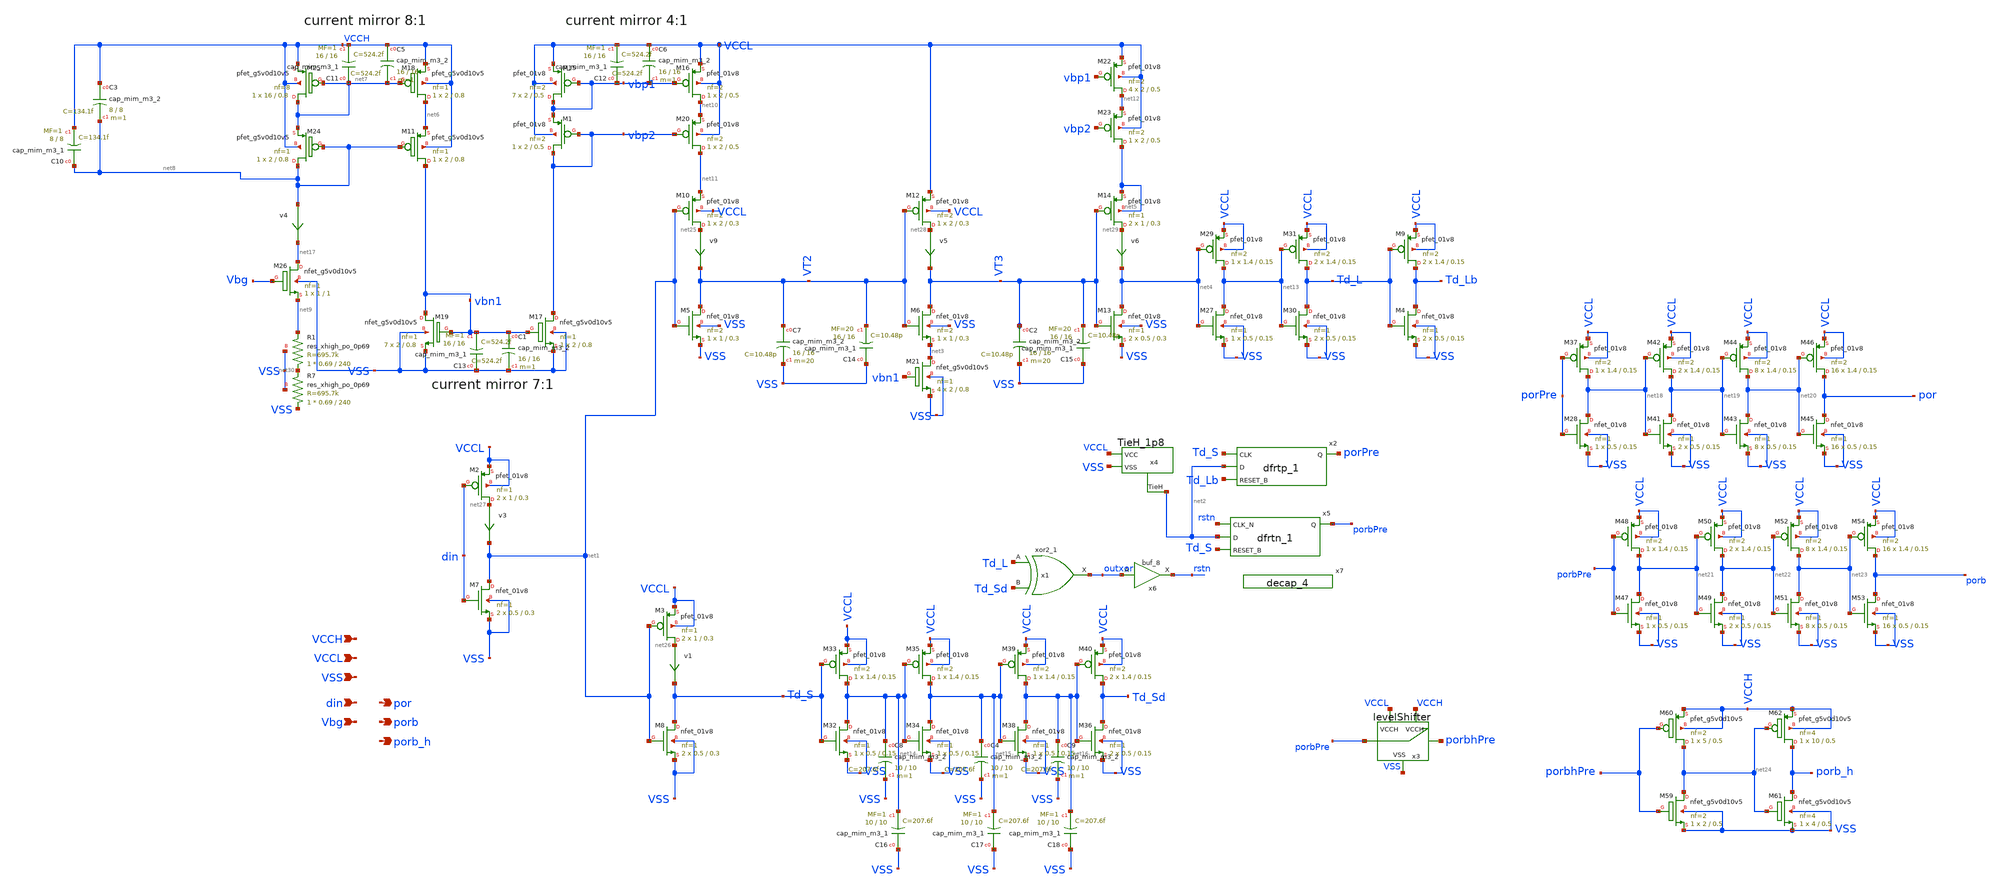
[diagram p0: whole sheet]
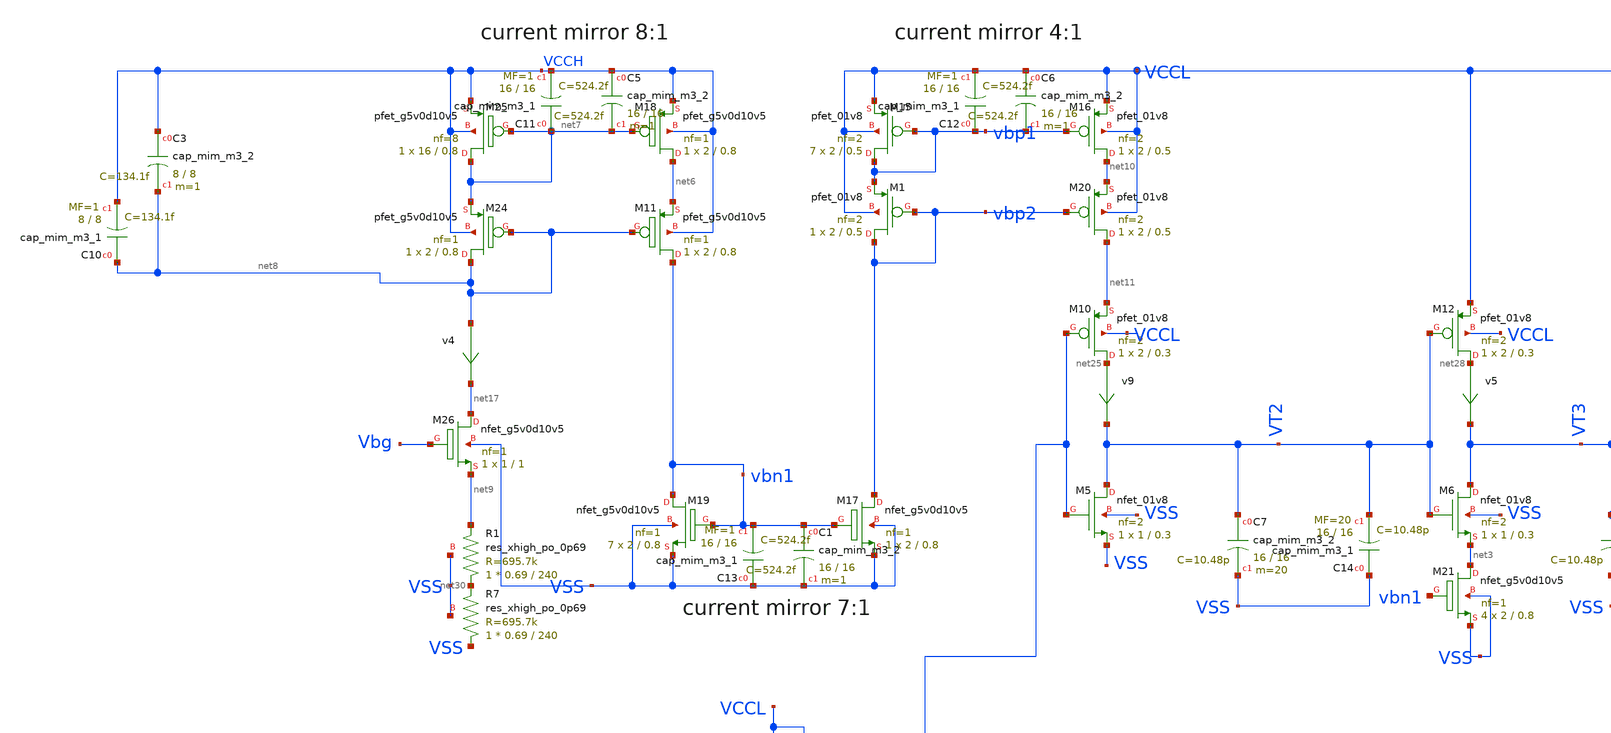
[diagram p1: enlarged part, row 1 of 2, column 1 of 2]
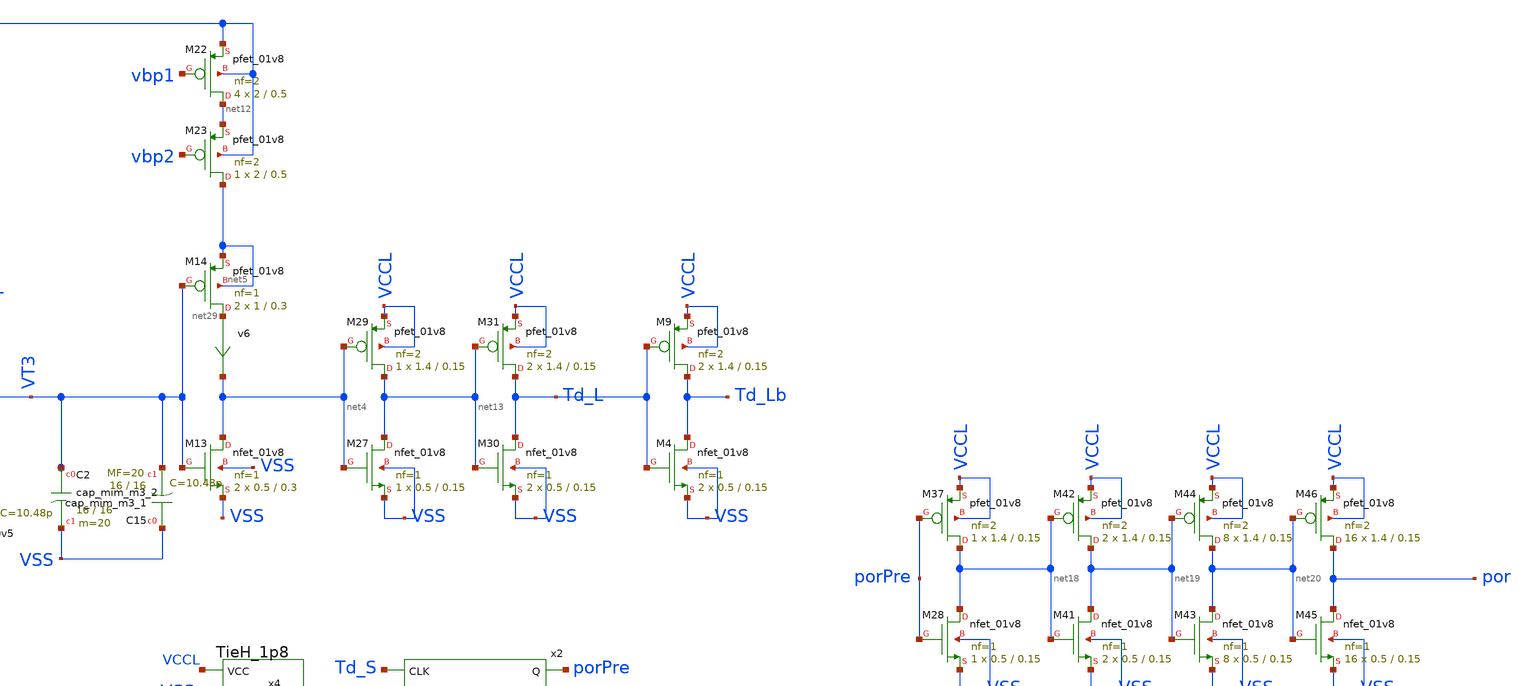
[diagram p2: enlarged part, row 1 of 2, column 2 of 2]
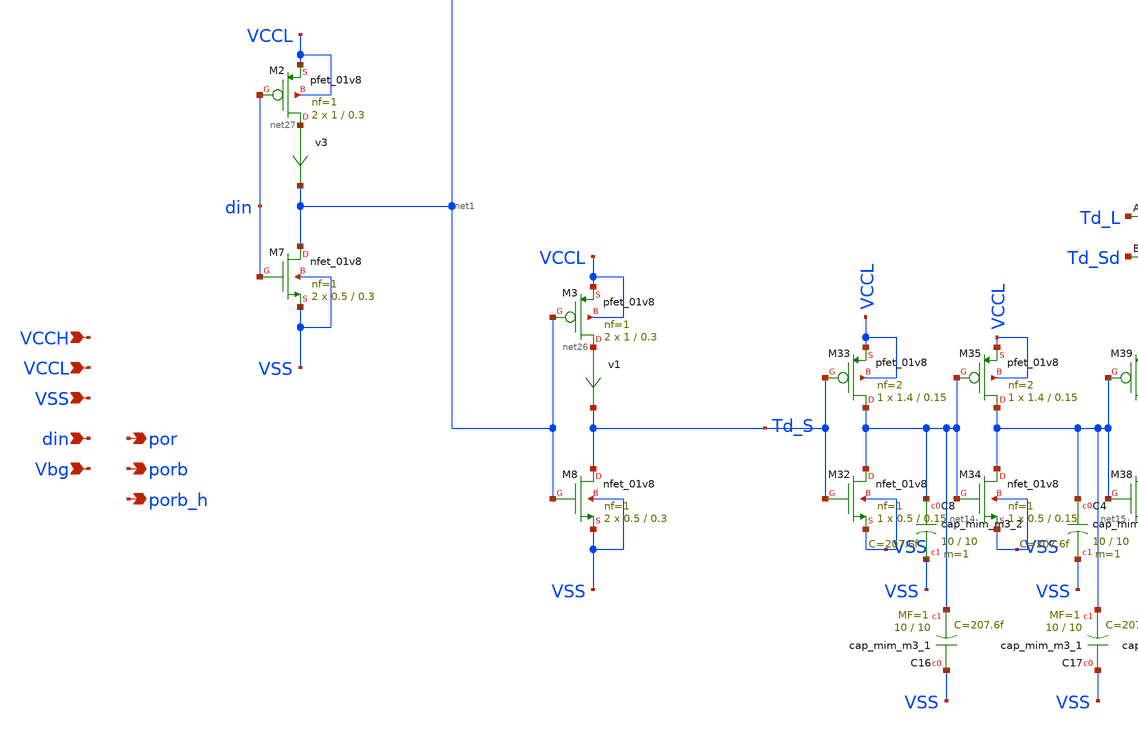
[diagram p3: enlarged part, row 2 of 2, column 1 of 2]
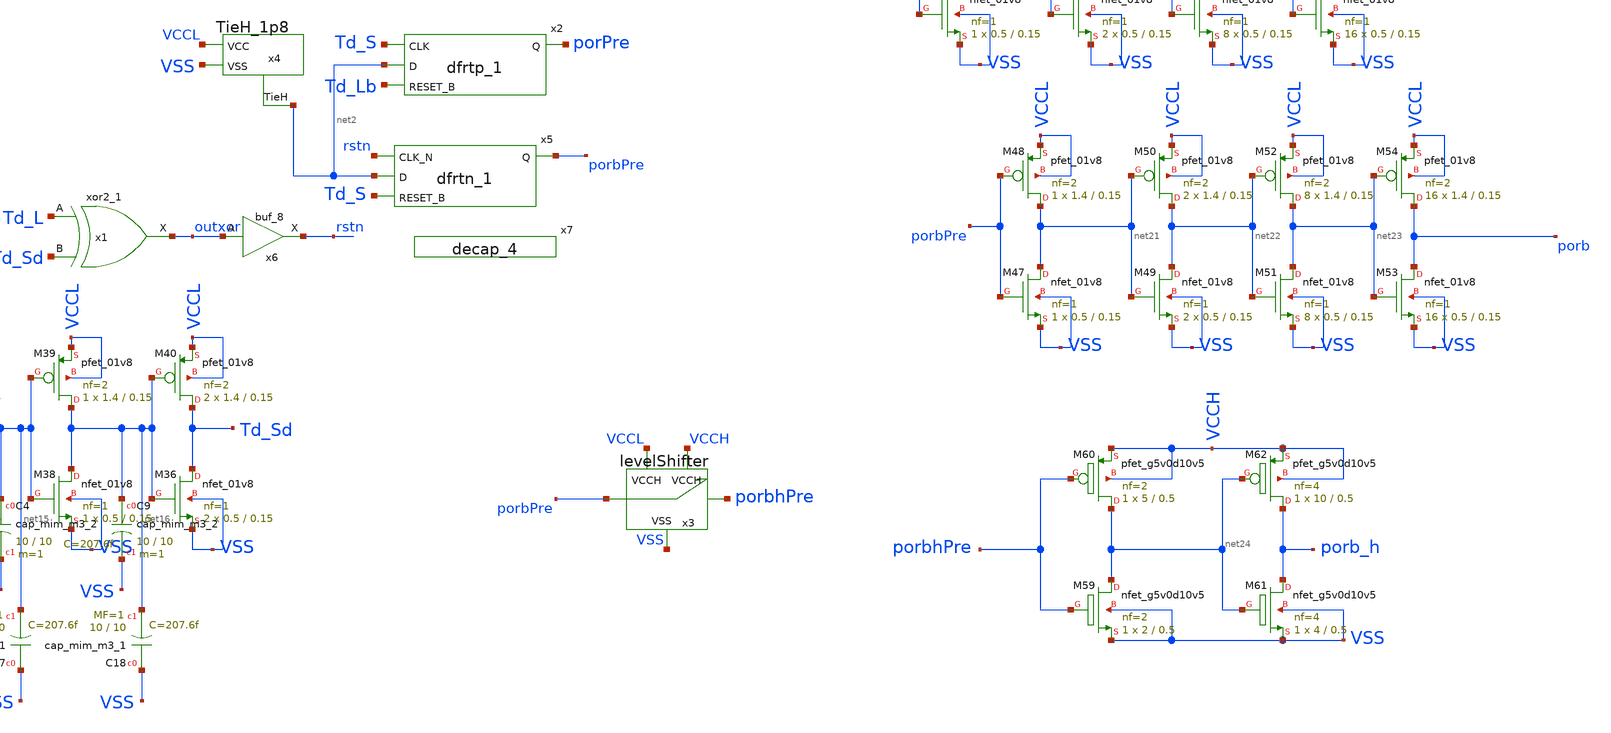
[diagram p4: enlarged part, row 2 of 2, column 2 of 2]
** sch_path: xschem_sim/delayPulse_final.sch
**.subckt delayPulse_final VCCL VSS din Vbg por VCCH porb porb_h
*.ipin VCCL
*.ipin VSS
*.ipin din
*.ipin Vbg
*.opin por
*.ipin VCCH
*.opin porb
*.opin porb_h
v9 net25 VT2 0
.save i(v9)
v1 net26 Td_S 0
.save i(v1)
v3 net27 net1 0
.save i(v3)
x1 Td_L Td_Sd VSS VSS VCCL VCCL outxor sky130_fd_sc_ls__xor2_1
x3 porbPre porbhPre VCCL VSS VCCH levelShifter
XM2 net27 din VCCL VCCL sky130_fd_pr__pfet_01v8 L=0.3 W=1 nf=1 ad='int((nf+1)/2) * W/nf * 0.29' as='int((nf+2)/2) * W/nf * 0.29'
+ pd='2*int((nf+1)/2) * (W/nf + 0.29)' ps='2*int((nf+2)/2) * (W/nf + 0.29)' nrd='0.29 / W' nrs='0.29 / W'
+ sa=0 sb=0 sd=0 mult=2 m=2
XM3 net26 net1 VCCL VCCL sky130_fd_pr__pfet_01v8 L=0.3 W=1 nf=1 ad='int((nf+1)/2) * W/nf * 0.29' as='int((nf+2)/2) * W/nf * 0.29'
+ pd='2*int((nf+1)/2) * (W/nf + 0.29)' ps='2*int((nf+2)/2) * (W/nf + 0.29)' nrd='0.29 / W' nrs='0.29 / W'
+ sa=0 sb=0 sd=0 mult=2 m=2
XM5 VT2 net1 VSS VSS sky130_fd_pr__nfet_01v8 L=0.3 W=1 nf=2 ad='int((nf+1)/2) * W/nf * 0.29' as='int((nf+2)/2) * W/nf * 0.29'
+ pd='2*int((nf+1)/2) * (W/nf + 0.29)' ps='2*int((nf+2)/2) * (W/nf + 0.29)' nrd='0.29 / W' nrs='0.29 / W'
+ sa=0 sb=0 sd=0 mult=1 m=1
XM7 net1 din VSS VSS sky130_fd_pr__nfet_01v8 L=0.3 W=0.5 nf=1 ad='int((nf+1)/2) * W/nf * 0.29' as='int((nf+2)/2) * W/nf * 0.29'
+ pd='2*int((nf+1)/2) * (W/nf + 0.29)' ps='2*int((nf+2)/2) * (W/nf + 0.29)' nrd='0.29 / W' nrs='0.29 / W'
+ sa=0 sb=0 sd=0 mult=2 m=2
XM8 Td_S net1 VSS VSS sky130_fd_pr__nfet_01v8 L=0.3 W=0.5 nf=1 ad='int((nf+1)/2) * W/nf * 0.29' as='int((nf+2)/2) * W/nf * 0.29'
+ pd='2*int((nf+1)/2) * (W/nf + 0.29)' ps='2*int((nf+2)/2) * (W/nf + 0.29)' nrd='0.29 / W' nrs='0.29 / W'
+ sa=0 sb=0 sd=0 mult=2 m=2
XM10 net25 net1 net11 VCCL sky130_fd_pr__pfet_01v8 L=0.3 W=2 nf=2 ad='int((nf+1)/2) * W/nf * 0.29' as='int((nf+2)/2) * W/nf * 0.29'
+ pd='2*int((nf+1)/2) * (W/nf + 0.29)' ps='2*int((nf+2)/2) * (W/nf + 0.29)' nrd='0.29 / W' nrs='0.29 / W'
+ sa=0 sb=0 sd=0 mult=1 m=1
v5 net28 VT3 0
.save i(v5)
v6 net29 net4 0
.save i(v6)
XM13 net4 VT3 VSS VSS sky130_fd_pr__nfet_01v8 L=0.3 W=0.5 nf=1 ad='int((nf+1)/2) * W/nf * 0.29' as='int((nf+2)/2) * W/nf * 0.29'
+ pd='2*int((nf+1)/2) * (W/nf + 0.29)' ps='2*int((nf+2)/2) * (W/nf + 0.29)' nrd='0.29 / W' nrs='0.29 / W'
+ sa=0 sb=0 sd=0 mult=2 m=2
XM14 net29 VT3 net5 net5 sky130_fd_pr__pfet_01v8 L=0.3 W=1 nf=1 ad='int((nf+1)/2) * W/nf * 0.29' as='int((nf+2)/2) * W/nf * 0.29'
+ pd='2*int((nf+1)/2) * (W/nf + 0.29)' ps='2*int((nf+2)/2) * (W/nf + 0.29)' nrd='0.29 / W' nrs='0.29 / W'
+ sa=0 sb=0 sd=0 mult=2 m=2
x4 net2 VSS VCCL TieH_1p8
XM11 vbn1 net8 net6 VCCH sky130_fd_pr__pfet_g5v0d10v5 L=0.8 W=2 nf=1 ad='int((nf+1)/2) * W/nf * 0.29'
+ as='int((nf+2)/2) * W/nf * 0.29' pd='2*int((nf+1)/2) * (W/nf + 0.29)' ps='2*int((nf+2)/2) * (W/nf + 0.29)'
+ nrd='0.29 / W' nrs='0.29 / W' sa=0 sb=0 sd=0 mult=1 m=1
XM17 vbp2 vbn1 VSS VSS sky130_fd_pr__nfet_g5v0d10v5 L=0.8 W=2 nf=1 ad='int((nf+1)/2) * W/nf * 0.29' as='int((nf+2)/2) * W/nf * 0.29'
+ pd='2*int((nf+1)/2) * (W/nf + 0.29)' ps='2*int((nf+2)/2) * (W/nf + 0.29)' nrd='0.29 / W' nrs='0.29 / W'
+ sa=0 sb=0 sd=0 mult=1 m=1
XM18 net6 net7 VCCH VCCH sky130_fd_pr__pfet_g5v0d10v5 L=0.8 W=2 nf=1 ad='int((nf+1)/2) * W/nf * 0.29'
+ as='int((nf+2)/2) * W/nf * 0.29' pd='2*int((nf+1)/2) * (W/nf + 0.29)' ps='2*int((nf+2)/2) * (W/nf + 0.29)'
+ nrd='0.29 / W' nrs='0.29 / W' sa=0 sb=0 sd=0 mult=1 m=1
XM19 vbn1 vbn1 VSS VSS sky130_fd_pr__nfet_g5v0d10v5 L=0.8 W=2 nf=1 ad='int((nf+1)/2) * W/nf * 0.29' as='int((nf+2)/2) * W/nf * 0.29'
+ pd='2*int((nf+1)/2) * (W/nf + 0.29)' ps='2*int((nf+2)/2) * (W/nf + 0.29)' nrd='0.29 / W' nrs='0.29 / W'
+ sa=0 sb=0 sd=0 mult=7 m=7
XM24 net8 net8 net7 VCCH sky130_fd_pr__pfet_g5v0d10v5 L=0.8 W=2 nf=1 ad='int((nf+1)/2) * W/nf * 0.29'
+ as='int((nf+2)/2) * W/nf * 0.29' pd='2*int((nf+1)/2) * (W/nf + 0.29)' ps='2*int((nf+2)/2) * (W/nf + 0.29)'
+ nrd='0.29 / W' nrs='0.29 / W' sa=0 sb=0 sd=0 mult=1 m=1
XM25 net7 net7 VCCH VCCH sky130_fd_pr__pfet_g5v0d10v5 L=0.8 W=16 nf=8 ad='int((nf+1)/2) * W/nf * 0.29'
+ as='int((nf+2)/2) * W/nf * 0.29' pd='2*int((nf+1)/2) * (W/nf + 0.29)' ps='2*int((nf+2)/2) * (W/nf + 0.29)'
+ nrd='0.29 / W' nrs='0.29 / W' sa=0 sb=0 sd=0 mult=1 m=1
XM26 net17 Vbg net9 VSS sky130_fd_pr__nfet_g5v0d10v5 L=1 W=1 nf=1 ad='int((nf+1)/2) * W/nf * 0.29' as='int((nf+2)/2) * W/nf * 0.29'
+ pd='2*int((nf+1)/2) * (W/nf + 0.29)' ps='2*int((nf+2)/2) * (W/nf + 0.29)' nrd='0.29 / W' nrs='0.29 / W'
+ sa=0 sb=0 sd=0 mult=1 m=1
XM6 VT3 VT2 net3 VSS sky130_fd_pr__nfet_01v8 L=0.3 W=1 nf=2 ad='int((nf+1)/2) * W/nf * 0.29' as='int((nf+2)/2) * W/nf * 0.29'
+ pd='2*int((nf+1)/2) * (W/nf + 0.29)' ps='2*int((nf+2)/2) * (W/nf + 0.29)' nrd='0.29 / W' nrs='0.29 / W'
+ sa=0 sb=0 sd=0 mult=1 m=1
XM12 net28 VT2 VCCL VCCL sky130_fd_pr__pfet_01v8 L=0.3 W=2 nf=2 ad='int((nf+1)/2) * W/nf * 0.29' as='int((nf+2)/2) * W/nf * 0.29'
+ pd='2*int((nf+1)/2) * (W/nf + 0.29)' ps='2*int((nf+2)/2) * (W/nf + 0.29)' nrd='0.29 / W' nrs='0.29 / W'
+ sa=0 sb=0 sd=0 mult=1 m=1
XM1 vbp2 vbp2 vbp1 VCCL sky130_fd_pr__pfet_01v8 L=0.5 W=2 nf=2 ad='int((nf+1)/2) * W/nf * 0.29' as='int((nf+2)/2) * W/nf * 0.29'
+ pd='2*int((nf+1)/2) * (W/nf + 0.29)' ps='2*int((nf+2)/2) * (W/nf + 0.29)' nrd='0.29 / W' nrs='0.29 / W'
+ sa=0 sb=0 sd=0 mult=1 m=1
XM15 vbp1 vbp1 VCCL VCCL sky130_fd_pr__pfet_01v8 L=0.5 W=2 nf=2 ad='int((nf+1)/2) * W/nf * 0.29' as='int((nf+2)/2) * W/nf * 0.29'
+ pd='2*int((nf+1)/2) * (W/nf + 0.29)' ps='2*int((nf+2)/2) * (W/nf + 0.29)' nrd='0.29 / W' nrs='0.29 / W'
+ sa=0 sb=0 sd=0 mult=7 m=7
XM16 net10 vbp1 VCCL VCCL sky130_fd_pr__pfet_01v8 L=0.5 W=2 nf=2 ad='int((nf+1)/2) * W/nf * 0.29' as='int((nf+2)/2) * W/nf * 0.29'
+ pd='2*int((nf+1)/2) * (W/nf + 0.29)' ps='2*int((nf+2)/2) * (W/nf + 0.29)' nrd='0.29 / W' nrs='0.29 / W'
+ sa=0 sb=0 sd=0 mult=1 m=1
XM20 net11 vbp2 net10 VCCL sky130_fd_pr__pfet_01v8 L=0.5 W=2 nf=2 ad='int((nf+1)/2) * W/nf * 0.29' as='int((nf+2)/2) * W/nf * 0.29'
+ pd='2*int((nf+1)/2) * (W/nf + 0.29)' ps='2*int((nf+2)/2) * (W/nf + 0.29)' nrd='0.29 / W' nrs='0.29 / W'
+ sa=0 sb=0 sd=0 mult=1 m=1
XM21 net3 vbn1 VSS VSS sky130_fd_pr__nfet_g5v0d10v5 L=0.8 W=2 nf=1 ad='int((nf+1)/2) * W/nf * 0.29' as='int((nf+2)/2) * W/nf * 0.29'
+ pd='2*int((nf+1)/2) * (W/nf + 0.29)' ps='2*int((nf+2)/2) * (W/nf + 0.29)' nrd='0.29 / W' nrs='0.29 / W'
+ sa=0 sb=0 sd=0 mult=4 m=4
XM22 net12 vbp1 VCCL VCCL sky130_fd_pr__pfet_01v8 L=0.5 W=2 nf=2 ad='int((nf+1)/2) * W/nf * 0.29' as='int((nf+2)/2) * W/nf * 0.29'
+ pd='2*int((nf+1)/2) * (W/nf + 0.29)' ps='2*int((nf+2)/2) * (W/nf + 0.29)' nrd='0.29 / W' nrs='0.29 / W'
+ sa=0 sb=0 sd=0 mult=4 m=4
XM23 net5 vbp2 net12 VCCL sky130_fd_pr__pfet_01v8 L=0.5 W=2 nf=2 ad='int((nf+1)/2) * W/nf * 0.29' as='int((nf+2)/2) * W/nf * 0.29'
+ pd='2*int((nf+1)/2) * (W/nf + 0.29)' ps='2*int((nf+2)/2) * (W/nf + 0.29)' nrd='0.29 / W' nrs='0.29 / W'
+ sa=0 sb=0 sd=0 mult=1 m=1
XM27 net13 net4 VSS VSS sky130_fd_pr__nfet_01v8 L=0.15 W=0.5 nf=1 ad='int((nf+1)/2) * W/nf * 0.29' as='int((nf+2)/2) * W/nf * 0.29'
+ pd='2*int((nf+1)/2) * (W/nf + 0.29)' ps='2*int((nf+2)/2) * (W/nf + 0.29)' nrd='0.29 / W' nrs='0.29 / W'
+ sa=0 sb=0 sd=0 mult=1 m=1
XM29 net13 net4 VCCL VCCL sky130_fd_pr__pfet_01v8 L=0.15 W=1.4 nf=2 ad='int((nf+1)/2) * W/nf * 0.29'
+ as='int((nf+2)/2) * W/nf * 0.29' pd='2*int((nf+1)/2) * (W/nf + 0.29)' ps='2*int((nf+2)/2) * (W/nf + 0.29)'
+ nrd='0.29 / W' nrs='0.29 / W' sa=0 sb=0 sd=0 mult=1 m=1
XM30 Td_L net13 VSS VSS sky130_fd_pr__nfet_01v8 L=0.15 W=0.5 nf=1 ad='int((nf+1)/2) * W/nf * 0.29' as='int((nf+2)/2) * W/nf * 0.29'
+ pd='2*int((nf+1)/2) * (W/nf + 0.29)' ps='2*int((nf+2)/2) * (W/nf + 0.29)' nrd='0.29 / W' nrs='0.29 / W'
+ sa=0 sb=0 sd=0 mult=2 m=2
XM31 Td_L net13 VCCL VCCL sky130_fd_pr__pfet_01v8 L=0.15 W=1.4 nf=2 ad='int((nf+1)/2) * W/nf * 0.29'
+ as='int((nf+2)/2) * W/nf * 0.29' pd='2*int((nf+1)/2) * (W/nf + 0.29)' ps='2*int((nf+2)/2) * (W/nf + 0.29)'
+ nrd='0.29 / W' nrs='0.29 / W' sa=0 sb=0 sd=0 mult=2 m=2
XM32 net14 Td_S VSS VSS sky130_fd_pr__nfet_01v8 L=0.15 W=0.5 nf=1 ad='int((nf+1)/2) * W/nf * 0.29' as='int((nf+2)/2) * W/nf * 0.29'
+ pd='2*int((nf+1)/2) * (W/nf + 0.29)' ps='2*int((nf+2)/2) * (W/nf + 0.29)' nrd='0.29 / W' nrs='0.29 / W'
+ sa=0 sb=0 sd=0 mult=1 m=1
XM33 net14 Td_S VCCL VCCL sky130_fd_pr__pfet_01v8 L=0.15 W=1.4 nf=2 ad='int((nf+1)/2) * W/nf * 0.29'
+ as='int((nf+2)/2) * W/nf * 0.29' pd='2*int((nf+1)/2) * (W/nf + 0.29)' ps='2*int((nf+2)/2) * (W/nf + 0.29)'
+ nrd='0.29 / W' nrs='0.29 / W' sa=0 sb=0 sd=0 mult=1 m=1
XM34 net15 net14 VSS VSS sky130_fd_pr__nfet_01v8 L=0.15 W=0.5 nf=1 ad='int((nf+1)/2) * W/nf * 0.29' as='int((nf+2)/2) * W/nf * 0.29'
+ pd='2*int((nf+1)/2) * (W/nf + 0.29)' ps='2*int((nf+2)/2) * (W/nf + 0.29)' nrd='0.29 / W' nrs='0.29 / W'
+ sa=0 sb=0 sd=0 mult=1 m=1
XM35 net15 net14 VCCL VCCL sky130_fd_pr__pfet_01v8 L=0.15 W=1.4 nf=2 ad='int((nf+1)/2) * W/nf * 0.29'
+ as='int((nf+2)/2) * W/nf * 0.29' pd='2*int((nf+1)/2) * (W/nf + 0.29)' ps='2*int((nf+2)/2) * (W/nf + 0.29)'
+ nrd='0.29 / W' nrs='0.29 / W' sa=0 sb=0 sd=0 mult=1 m=1
XM36 Td_Sd net16 VSS VSS sky130_fd_pr__nfet_01v8 L=0.15 W=0.5 nf=1 ad='int((nf+1)/2) * W/nf * 0.29' as='int((nf+2)/2) * W/nf * 0.29'
+ pd='2*int((nf+1)/2) * (W/nf + 0.29)' ps='2*int((nf+2)/2) * (W/nf + 0.29)' nrd='0.29 / W' nrs='0.29 / W'
+ sa=0 sb=0 sd=0 mult=2 m=2
XM38 net16 net15 VSS VSS sky130_fd_pr__nfet_01v8 L=0.15 W=0.5 nf=1 ad='int((nf+1)/2) * W/nf * 0.29' as='int((nf+2)/2) * W/nf * 0.29'
+ pd='2*int((nf+1)/2) * (W/nf + 0.29)' ps='2*int((nf+2)/2) * (W/nf + 0.29)' nrd='0.29 / W' nrs='0.29 / W'
+ sa=0 sb=0 sd=0 mult=1 m=1
XM39 net16 net15 VCCL VCCL sky130_fd_pr__pfet_01v8 L=0.15 W=1.4 nf=2 ad='int((nf+1)/2) * W/nf * 0.29'
+ as='int((nf+2)/2) * W/nf * 0.29' pd='2*int((nf+1)/2) * (W/nf + 0.29)' ps='2*int((nf+2)/2) * (W/nf + 0.29)'
+ nrd='0.29 / W' nrs='0.29 / W' sa=0 sb=0 sd=0 mult=1 m=1
x6 outxor VSS VSS VCCL VCCL rstn sky130_fd_sc_ls__buf_8
XC4 net15 VSS sky130_fd_pr__cap_mim_m3_2 W=10 L=10 MF=1 m=1
XC7 VT2 VSS sky130_fd_pr__cap_mim_m3_2 W=16 L=16 MF=20 m=20
XC2 VT3 VSS sky130_fd_pr__cap_mim_m3_2 W=16 L=16 MF=20 m=20
XC8 net14 VSS sky130_fd_pr__cap_mim_m3_2 W=10 L=10 MF=1 m=1
XC9 net16 VSS sky130_fd_pr__cap_mim_m3_2 W=10 L=10 MF=1 m=1
XM40 Td_Sd net16 VCCL VCCL sky130_fd_pr__pfet_01v8 L=0.15 W=1.4 nf=2 ad='int((nf+1)/2) * W/nf * 0.29'
+ as='int((nf+2)/2) * W/nf * 0.29' pd='2*int((nf+1)/2) * (W/nf + 0.29)' ps='2*int((nf+2)/2) * (W/nf + 0.29)'
+ nrd='0.29 / W' nrs='0.29 / W' sa=0 sb=0 sd=0 mult=2 m=2
v4 net8 net17 0
.save i(v4)
x5 rstn net2 Td_S VSS VSS VCCL VCCL porbPre sky130_fd_sc_ls__dfrtn_1
x2 Td_S net2 Td_Lb VSS VSS VCCL VCCL porPre sky130_fd_sc_ls__dfrtp_1
XM4 Td_Lb Td_L VSS VSS sky130_fd_pr__nfet_01v8 L=0.15 W=0.5 nf=1 ad='int((nf+1)/2) * W/nf * 0.29' as='int((nf+2)/2) * W/nf * 0.29'
+ pd='2*int((nf+1)/2) * (W/nf + 0.29)' ps='2*int((nf+2)/2) * (W/nf + 0.29)' nrd='0.29 / W' nrs='0.29 / W'
+ sa=0 sb=0 sd=0 mult=2 m=2
XM9 Td_Lb Td_L VCCL VCCL sky130_fd_pr__pfet_01v8 L=0.15 W=1.4 nf=2 ad='int((nf+1)/2) * W/nf * 0.29' as='int((nf+2)/2) * W/nf * 0.29'
+ pd='2*int((nf+1)/2) * (W/nf + 0.29)' ps='2*int((nf+2)/2) * (W/nf + 0.29)' nrd='0.29 / W' nrs='0.29 / W'
+ sa=0 sb=0 sd=0 mult=2 m=2
XC1 vbn1 VSS sky130_fd_pr__cap_mim_m3_2 W=16 L=16 MF=1 m=1
XC5 VCCH net7 sky130_fd_pr__cap_mim_m3_2 W=16 L=16 MF=1 m=1
XC6 VCCL vbp1 sky130_fd_pr__cap_mim_m3_2 W=16 L=16 MF=1 m=1
XC3 VCCH net8 sky130_fd_pr__cap_mim_m3_2 W=8 L=8 MF=1 m=1
XM28 net18 porPre VSS VSS sky130_fd_pr__nfet_01v8 L=0.15 W=0.5 nf=1 ad='int((nf+1)/2) * W/nf * 0.29'
+ as='int((nf+2)/2) * W/nf * 0.29' pd='2*int((nf+1)/2) * (W/nf + 0.29)' ps='2*int((nf+2)/2) * (W/nf + 0.29)'
+ nrd='0.29 / W' nrs='0.29 / W' sa=0 sb=0 sd=0 mult=1 m=1
XM37 net18 porPre VCCL VCCL sky130_fd_pr__pfet_01v8 L=0.15 W=1.4 nf=2 ad='int((nf+1)/2) * W/nf * 0.29'
+ as='int((nf+2)/2) * W/nf * 0.29' pd='2*int((nf+1)/2) * (W/nf + 0.29)' ps='2*int((nf+2)/2) * (W/nf + 0.29)'
+ nrd='0.29 / W' nrs='0.29 / W' sa=0 sb=0 sd=0 mult=1 m=1
XM41 net19 net18 VSS VSS sky130_fd_pr__nfet_01v8 L=0.15 W=0.5 nf=1 ad='int((nf+1)/2) * W/nf * 0.29' as='int((nf+2)/2) * W/nf * 0.29'
+ pd='2*int((nf+1)/2) * (W/nf + 0.29)' ps='2*int((nf+2)/2) * (W/nf + 0.29)' nrd='0.29 / W' nrs='0.29 / W'
+ sa=0 sb=0 sd=0 mult=2 m=2
XM42 net19 net18 VCCL VCCL sky130_fd_pr__pfet_01v8 L=0.15 W=1.4 nf=2 ad='int((nf+1)/2) * W/nf * 0.29'
+ as='int((nf+2)/2) * W/nf * 0.29' pd='2*int((nf+1)/2) * (W/nf + 0.29)' ps='2*int((nf+2)/2) * (W/nf + 0.29)'
+ nrd='0.29 / W' nrs='0.29 / W' sa=0 sb=0 sd=0 mult=2 m=2
XM43 net20 net19 VSS VSS sky130_fd_pr__nfet_01v8 L=0.15 W=0.5 nf=1 ad='int((nf+1)/2) * W/nf * 0.29' as='int((nf+2)/2) * W/nf * 0.29'
+ pd='2*int((nf+1)/2) * (W/nf + 0.29)' ps='2*int((nf+2)/2) * (W/nf + 0.29)' nrd='0.29 / W' nrs='0.29 / W'
+ sa=0 sb=0 sd=0 mult=8 m=8
XM44 net20 net19 VCCL VCCL sky130_fd_pr__pfet_01v8 L=0.15 W=1.4 nf=2 ad='int((nf+1)/2) * W/nf * 0.29'
+ as='int((nf+2)/2) * W/nf * 0.29' pd='2*int((nf+1)/2) * (W/nf + 0.29)' ps='2*int((nf+2)/2) * (W/nf + 0.29)'
+ nrd='0.29 / W' nrs='0.29 / W' sa=0 sb=0 sd=0 mult=8 m=8
XM45 por net20 VSS VSS sky130_fd_pr__nfet_01v8 L=0.15 W=0.5 nf=1 ad='int((nf+1)/2) * W/nf * 0.29' as='int((nf+2)/2) * W/nf * 0.29'
+ pd='2*int((nf+1)/2) * (W/nf + 0.29)' ps='2*int((nf+2)/2) * (W/nf + 0.29)' nrd='0.29 / W' nrs='0.29 / W'
+ sa=0 sb=0 sd=0 mult=16 m=16
XM46 por net20 VCCL VCCL sky130_fd_pr__pfet_01v8 L=0.15 W=1.4 nf=2 ad='int((nf+1)/2) * W/nf * 0.29' as='int((nf+2)/2) * W/nf * 0.29'
+ pd='2*int((nf+1)/2) * (W/nf + 0.29)' ps='2*int((nf+2)/2) * (W/nf + 0.29)' nrd='0.29 / W' nrs='0.29 / W'
+ sa=0 sb=0 sd=0 mult=16 m=16
XM47 net21 porbPre VSS VSS sky130_fd_pr__nfet_01v8 L=0.15 W=0.5 nf=1 ad='int((nf+1)/2) * W/nf * 0.29'
+ as='int((nf+2)/2) * W/nf * 0.29' pd='2*int((nf+1)/2) * (W/nf + 0.29)' ps='2*int((nf+2)/2) * (W/nf + 0.29)'
+ nrd='0.29 / W' nrs='0.29 / W' sa=0 sb=0 sd=0 mult=1 m=1
XM48 net21 porbPre VCCL VCCL sky130_fd_pr__pfet_01v8 L=0.15 W=1.4 nf=2 ad='int((nf+1)/2) * W/nf * 0.29'
+ as='int((nf+2)/2) * W/nf * 0.29' pd='2*int((nf+1)/2) * (W/nf + 0.29)' ps='2*int((nf+2)/2) * (W/nf + 0.29)'
+ nrd='0.29 / W' nrs='0.29 / W' sa=0 sb=0 sd=0 mult=1 m=1
XM49 net22 net21 VSS VSS sky130_fd_pr__nfet_01v8 L=0.15 W=0.5 nf=1 ad='int((nf+1)/2) * W/nf * 0.29' as='int((nf+2)/2) * W/nf * 0.29'
+ pd='2*int((nf+1)/2) * (W/nf + 0.29)' ps='2*int((nf+2)/2) * (W/nf + 0.29)' nrd='0.29 / W' nrs='0.29 / W'
+ sa=0 sb=0 sd=0 mult=2 m=2
XM50 net22 net21 VCCL VCCL sky130_fd_pr__pfet_01v8 L=0.15 W=1.4 nf=2 ad='int((nf+1)/2) * W/nf * 0.29'
+ as='int((nf+2)/2) * W/nf * 0.29' pd='2*int((nf+1)/2) * (W/nf + 0.29)' ps='2*int((nf+2)/2) * (W/nf + 0.29)'
+ nrd='0.29 / W' nrs='0.29 / W' sa=0 sb=0 sd=0 mult=2 m=2
XM51 net23 net22 VSS VSS sky130_fd_pr__nfet_01v8 L=0.15 W=0.5 nf=1 ad='int((nf+1)/2) * W/nf * 0.29' as='int((nf+2)/2) * W/nf * 0.29'
+ pd='2*int((nf+1)/2) * (W/nf + 0.29)' ps='2*int((nf+2)/2) * (W/nf + 0.29)' nrd='0.29 / W' nrs='0.29 / W'
+ sa=0 sb=0 sd=0 mult=8 m=8
XM52 net23 net22 VCCL VCCL sky130_fd_pr__pfet_01v8 L=0.15 W=1.4 nf=2 ad='int((nf+1)/2) * W/nf * 0.29'
+ as='int((nf+2)/2) * W/nf * 0.29' pd='2*int((nf+1)/2) * (W/nf + 0.29)' ps='2*int((nf+2)/2) * (W/nf + 0.29)'
+ nrd='0.29 / W' nrs='0.29 / W' sa=0 sb=0 sd=0 mult=8 m=8
XM53 porb net23 VSS VSS sky130_fd_pr__nfet_01v8 L=0.15 W=0.5 nf=1 ad='int((nf+1)/2) * W/nf * 0.29' as='int((nf+2)/2) * W/nf * 0.29'
+ pd='2*int((nf+1)/2) * (W/nf + 0.29)' ps='2*int((nf+2)/2) * (W/nf + 0.29)' nrd='0.29 / W' nrs='0.29 / W'
+ sa=0 sb=0 sd=0 mult=16 m=16
XM54 porb net23 VCCL VCCL sky130_fd_pr__pfet_01v8 L=0.15 W=1.4 nf=2 ad='int((nf+1)/2) * W/nf * 0.29'
+ as='int((nf+2)/2) * W/nf * 0.29' pd='2*int((nf+1)/2) * (W/nf + 0.29)' ps='2*int((nf+2)/2) * (W/nf + 0.29)'
+ nrd='0.29 / W' nrs='0.29 / W' sa=0 sb=0 sd=0 mult=16 m=16
XM59 net24 porbhPre VSS VSS sky130_fd_pr__nfet_g5v0d10v5 L=0.5 W=2 nf=2 ad='int((nf+1)/2) * W/nf * 0.29'
+ as='int((nf+2)/2) * W/nf * 0.29' pd='2*int((nf+1)/2) * (W/nf + 0.29)' ps='2*int((nf+2)/2) * (W/nf + 0.29)'
+ nrd='0.29 / W' nrs='0.29 / W' sa=0 sb=0 sd=0 mult=1 m=1
XM60 net24 porbhPre VCCH VCCH sky130_fd_pr__pfet_g5v0d10v5 L=0.5 W=5 nf=2 ad='int((nf+1)/2) * W/nf * 0.29'
+ as='int((nf+2)/2) * W/nf * 0.29' pd='2*int((nf+1)/2) * (W/nf + 0.29)' ps='2*int((nf+2)/2) * (W/nf + 0.29)'
+ nrd='0.29 / W' nrs='0.29 / W' sa=0 sb=0 sd=0 mult=1 m=1
XM61 porb_h net24 VSS VSS sky130_fd_pr__nfet_g5v0d10v5 L=0.5 W=4 nf=4 ad='int((nf+1)/2) * W/nf * 0.29'
+ as='int((nf+2)/2) * W/nf * 0.29' pd='2*int((nf+1)/2) * (W/nf + 0.29)' ps='2*int((nf+2)/2) * (W/nf + 0.29)'
+ nrd='0.29 / W' nrs='0.29 / W' sa=0 sb=0 sd=0 mult=1 m=1
XM62 porb_h net24 VCCH VCCH sky130_fd_pr__pfet_g5v0d10v5 L=0.5 W=10 nf=4 ad='int((nf+1)/2) * W/nf * 0.29'
+ as='int((nf+2)/2) * W/nf * 0.29' pd='2*int((nf+1)/2) * (W/nf + 0.29)' ps='2*int((nf+2)/2) * (W/nf + 0.29)'
+ nrd='0.29 / W' nrs='0.29 / W' sa=0 sb=0 sd=0 mult=1 m=1
x7 VSS VSS VCCL VCCL sky130_fd_sc_ls__decap_4
XC10 net8 VCCH sky130_fd_pr__cap_mim_m3_1 W=8 L=8 MF=1 m=1
XC11 net7 VCCH sky130_fd_pr__cap_mim_m3_1 W=16 L=16 MF=1 m=1
XC12 vbp1 VCCL sky130_fd_pr__cap_mim_m3_1 W=16 L=16 MF=1 m=1
XC13 VSS vbn1 sky130_fd_pr__cap_mim_m3_1 W=16 L=16 MF=1 m=1
XC14 VSS VT2 sky130_fd_pr__cap_mim_m3_1 W=16 L=16 MF=20 m=20
XC15 VSS VT3 sky130_fd_pr__cap_mim_m3_1 W=16 L=16 MF=20 m=20
XC16 VSS net14 sky130_fd_pr__cap_mim_m3_1 W=10 L=10 MF=1 m=1
XC17 VSS net15 sky130_fd_pr__cap_mim_m3_1 W=10 L=10 MF=1 m=1
XC18 VSS net16 sky130_fd_pr__cap_mim_m3_1 W=10 L=10 MF=1 m=1
XR1 net30 net9 VSS sky130_fd_pr__res_xhigh_po_0p69 L=240 mult=1 m=1
XR7 VSS net30 VSS sky130_fd_pr__res_xhigh_po_0p69 L=240 mult=1 m=1
**.ends
.end
